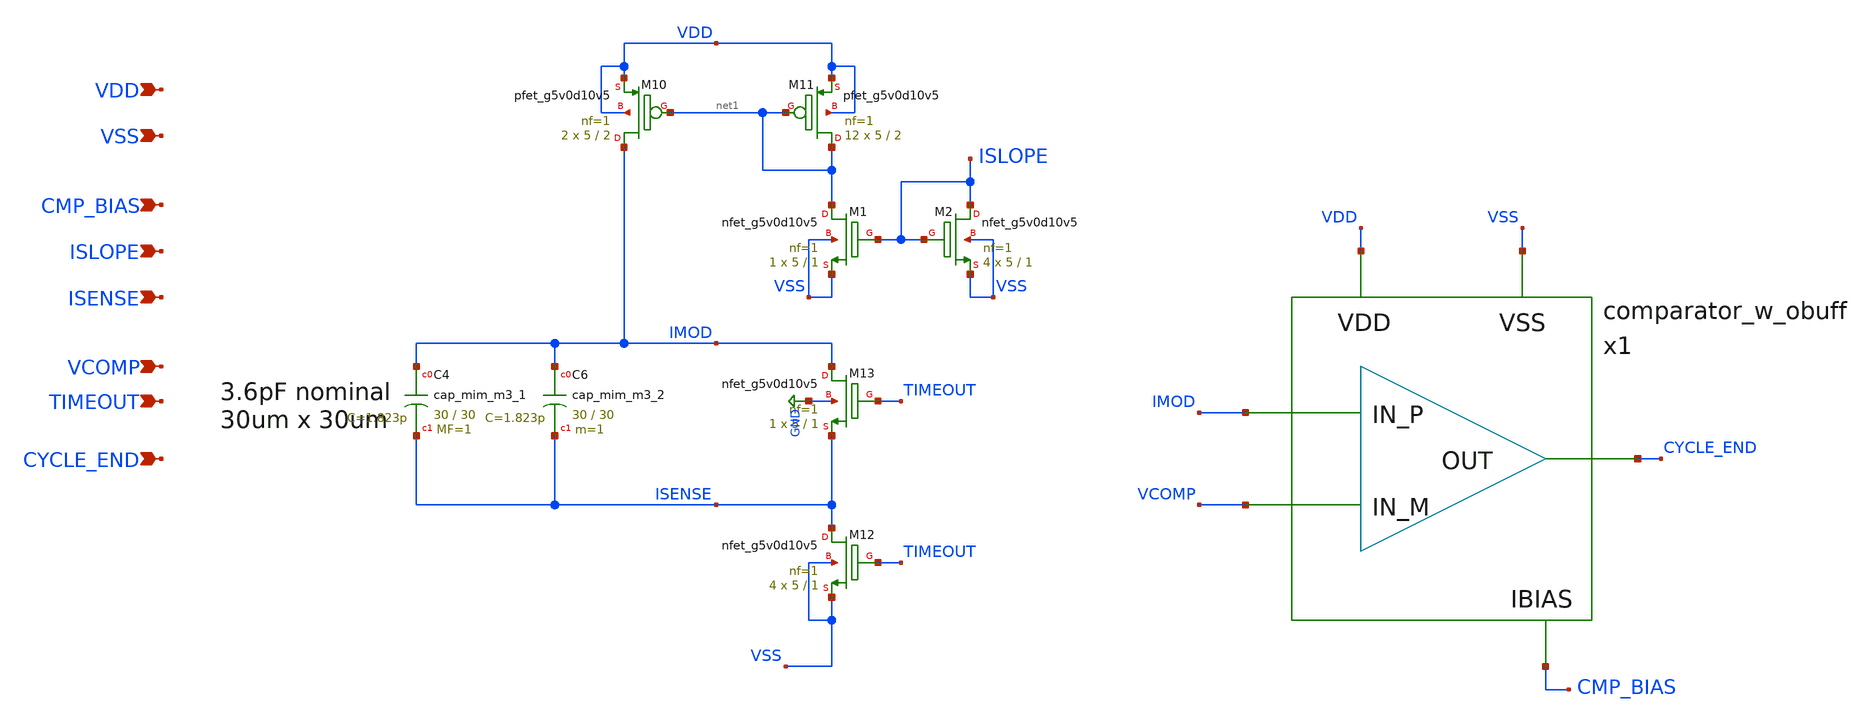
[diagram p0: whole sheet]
** sch_path: design/modulator/modulator.sch
**.subckt modulator ISENSE VCOMP TIMEOUT VDD VSS CMP_BIAS ISLOPE CYCLE_END
*.ipin ISENSE
*.ipin VCOMP
*.ipin TIMEOUT
*.ipin VDD
*.ipin VSS
*.ipin CMP_BIAS
*.ipin ISLOPE
*.ipin CYCLE_END
x1 IMOD VCOMP CYCLE_END VDD VSS CMP_BIAS comparator_w_obuff
XM10 IMOD net1 VDD VDD sky130_fd_pr__pfet_g5v0d10v5 L=2 W=5 nf=1 ad='int((nf+1)/2) * W/nf * 0.29' as='int((nf+2)/2) * W/nf * 0.29'
+ pd='2*int((nf+1)/2) * (W/nf + 0.29)' ps='2*int((nf+2)/2) * (W/nf + 0.29)' nrd='0.29 / W' nrs='0.29 / W'
+ sa=0 sb=0 sd=0 mult=2 m=2
XM11 net1 net1 VDD VDD sky130_fd_pr__pfet_g5v0d10v5 L=2 W=5 nf=1 ad='int((nf+1)/2) * W/nf * 0.29' as='int((nf+2)/2) * W/nf * 0.29'
+ pd='2*int((nf+1)/2) * (W/nf + 0.29)' ps='2*int((nf+2)/2) * (W/nf + 0.29)' nrd='0.29 / W' nrs='0.29 / W'
+ sa=0 sb=0 sd=0 mult=12 m=12
XM12 ISENSE TIMEOUT VSS VSS sky130_fd_pr__nfet_g5v0d10v5 L=1 W=5 nf=1 ad='int((nf+1)/2) * W/nf * 0.29'
+ as='int((nf+2)/2) * W/nf * 0.29' pd='2*int((nf+1)/2) * (W/nf + 0.29)' ps='2*int((nf+2)/2) * (W/nf + 0.29)'
+ nrd='0.29 / W' nrs='0.29 / W' sa=0 sb=0 sd=0 mult=4 m=4
XM13 IMOD TIMEOUT ISENSE GND sky130_fd_pr__nfet_g5v0d10v5 L=1 W=5 nf=1 ad='int((nf+1)/2) * W/nf * 0.29'
+ as='int((nf+2)/2) * W/nf * 0.29' pd='2*int((nf+1)/2) * (W/nf + 0.29)' ps='2*int((nf+2)/2) * (W/nf + 0.29)'
+ nrd='0.29 / W' nrs='0.29 / W' sa=0 sb=0 sd=0 mult=1 m=1
XC4 IMOD ISENSE sky130_fd_pr__cap_mim_m3_1 W=30 L=30 MF=1 m=1
XC6 IMOD ISENSE sky130_fd_pr__cap_mim_m3_2 W=30 L=30 MF=1 m=1
XM1 net1 ISLOPE VSS VSS sky130_fd_pr__nfet_g5v0d10v5 L=1 W=5 nf=1 ad='int((nf+1)/2) * W/nf * 0.29' as='int((nf+2)/2) * W/nf * 0.29'
+ pd='2*int((nf+1)/2) * (W/nf + 0.29)' ps='2*int((nf+2)/2) * (W/nf + 0.29)' nrd='0.29 / W' nrs='0.29 / W'
+ sa=0 sb=0 sd=0 mult=1 m=1
XM2 ISLOPE ISLOPE VSS VSS sky130_fd_pr__nfet_g5v0d10v5 L=1 W=5 nf=1 ad='int((nf+1)/2) * W/nf * 0.29'
+ as='int((nf+2)/2) * W/nf * 0.29' pd='2*int((nf+1)/2) * (W/nf + 0.29)' ps='2*int((nf+2)/2) * (W/nf + 0.29)'
+ nrd='0.29 / W' nrs='0.29 / W' sa=0 sb=0 sd=0 mult=4 m=4
**.ends

* expanding   symbol:  design/comparator/comparator_w_obuff.sym # of pins=6
** sym_path: design/comparator/comparator_w_obuff.sym
** sch_path: design/comparator/comparator_w_obuff.sch
.subckt comparator_w_obuff Vinp Vinm Vout VDD VSS IB
*.iopin VDD
*.iopin VSS
*.iopin Vout
*.iopin Vinp
*.iopin Vinm
*.iopin IB
XM11 net4 IB VDD VDD sky130_fd_pr__pfet_g5v0d10v5 L=1 W=5 nf=1 ad='int((nf+1)/2) * W/nf * 0.29' as='int((nf+2)/2) * W/nf * 0.29'
+ pd='2*int((nf+1)/2) * (W/nf + 0.29)' ps='2*int((nf+2)/2) * (W/nf + 0.29)' nrd='0.29 / W' nrs='0.29 / W'
+ sa=0 sb=0 sd=0 mult=4 m=4
XM8 VMID net1 VDD VDD sky130_fd_pr__pfet_g5v0d10v5 L=1 W=5 nf=1 ad='int((nf+1)/2) * W/nf * 0.29' as='int((nf+2)/2) * W/nf * 0.29'
+ pd='2*int((nf+1)/2) * (W/nf + 0.29)' ps='2*int((nf+2)/2) * (W/nf + 0.29)' nrd='0.29 / W' nrs='0.29 / W'
+ sa=0 sb=0 sd=0 mult=4 m=4
XM7 net1 net1 VDD VDD sky130_fd_pr__pfet_g5v0d10v5 L=1 W=5 nf=1 ad='int((nf+1)/2) * W/nf * 0.29' as='int((nf+2)/2) * W/nf * 0.29'
+ pd='2*int((nf+1)/2) * (W/nf + 0.29)' ps='2*int((nf+2)/2) * (W/nf + 0.29)' nrd='0.29 / W' nrs='0.29 / W'
+ sa=0 sb=0 sd=0 mult=4 m=4
XM2 net3 Vinm net4 VDD sky130_fd_pr__pfet_g5v0d10v5 L=1 W=5 nf=1 ad='int((nf+1)/2) * W/nf * 0.29' as='int((nf+2)/2) * W/nf * 0.29'
+ pd='2*int((nf+1)/2) * (W/nf + 0.29)' ps='2*int((nf+2)/2) * (W/nf + 0.29)' nrd='0.29 / W' nrs='0.29 / W'
+ sa=0 sb=0 sd=0 mult=4 m=4
XM1 net2 Vinp net4 VDD sky130_fd_pr__pfet_g5v0d10v5 L=1 W=5 nf=1 ad='int((nf+1)/2) * W/nf * 0.29' as='int((nf+2)/2) * W/nf * 0.29'
+ pd='2*int((nf+1)/2) * (W/nf + 0.29)' ps='2*int((nf+2)/2) * (W/nf + 0.29)' nrd='0.29 / W' nrs='0.29 / W'
+ sa=0 sb=0 sd=0 mult=4 m=4
XMmir IB IB VDD VDD sky130_fd_pr__pfet_g5v0d10v5 L=1 W=5 nf=1 ad='int((nf+1)/2) * W/nf * 0.29' as='int((nf+2)/2) * W/nf * 0.29'
+ pd='2*int((nf+1)/2) * (W/nf + 0.29)' ps='2*int((nf+2)/2) * (W/nf + 0.29)' nrd='0.29 / W' nrs='0.29 / W'
+ sa=0 sb=0 sd=0 mult=2 m=2
XM12 VMID net3 VSS VSS sky130_fd_pr__nfet_g5v0d10v5 L=1 W=5 nf=1 ad='int((nf+1)/2) * W/nf * 0.29' as='int((nf+2)/2) * W/nf * 0.29'
+ pd='2*int((nf+1)/2) * (W/nf + 0.29)' ps='2*int((nf+2)/2) * (W/nf + 0.29)' nrd='0.29 / W' nrs='0.29 / W'
+ sa=0 sb=0 sd=0 mult=4 m=4
XM4 net3 net3 VSS VSS sky130_fd_pr__nfet_g5v0d10v5 L=1 W=5 nf=1 ad='int((nf+1)/2) * W/nf * 0.29' as='int((nf+2)/2) * W/nf * 0.29'
+ pd='2*int((nf+1)/2) * (W/nf + 0.29)' ps='2*int((nf+2)/2) * (W/nf + 0.29)' nrd='0.29 / W' nrs='0.29 / W'
+ sa=0 sb=0 sd=0 mult=3 m=3
XM6 net2 net3 VSS VSS sky130_fd_pr__nfet_g5v0d10v5 L=1 W=5 nf=1 ad='int((nf+1)/2) * W/nf * 0.29' as='int((nf+2)/2) * W/nf * 0.29'
+ pd='2*int((nf+1)/2) * (W/nf + 0.29)' ps='2*int((nf+2)/2) * (W/nf + 0.29)' nrd='0.29 / W' nrs='0.29 / W'
+ sa=0 sb=0 sd=0 mult=4 m=4
XM5 net3 net2 VSS VSS sky130_fd_pr__nfet_g5v0d10v5 L=1 W=5 nf=1 ad='int((nf+1)/2) * W/nf * 0.29' as='int((nf+2)/2) * W/nf * 0.29'
+ pd='2*int((nf+1)/2) * (W/nf + 0.29)' ps='2*int((nf+2)/2) * (W/nf + 0.29)' nrd='0.29 / W' nrs='0.29 / W'
+ sa=0 sb=0 sd=0 mult=4 m=4
XM3 net2 net2 VSS VSS sky130_fd_pr__nfet_g5v0d10v5 L=1 W=5 nf=1 ad='int((nf+1)/2) * W/nf * 0.29' as='int((nf+2)/2) * W/nf * 0.29'
+ pd='2*int((nf+1)/2) * (W/nf + 0.29)' ps='2*int((nf+2)/2) * (W/nf + 0.29)' nrd='0.29 / W' nrs='0.29 / W'
+ sa=0 sb=0 sd=0 mult=3 m=3
XM9 net1 net2 VSS VSS sky130_fd_pr__nfet_g5v0d10v5 L=1 W=5 nf=1 ad='int((nf+1)/2) * W/nf * 0.29' as='int((nf+2)/2) * W/nf * 0.29'
+ pd='2*int((nf+1)/2) * (W/nf + 0.29)' ps='2*int((nf+2)/2) * (W/nf + 0.29)' nrd='0.29 / W' nrs='0.29 / W'
+ sa=0 sb=0 sd=0 mult=4 m=4
XM10 Vout VMID VDD VDD sky130_fd_pr__pfet_g5v0d10v5 L=0.5 W=5 nf=1 ad='int((nf+1)/2) * W/nf * 0.29' as='int((nf+2)/2) * W/nf * 0.29'
+ pd='2*int((nf+1)/2) * (W/nf + 0.29)' ps='2*int((nf+2)/2) * (W/nf + 0.29)' nrd='0.29 / W' nrs='0.29 / W'
+ sa=0 sb=0 sd=0 mult=1 m=1
XM13 Vout VMID VSS VSS sky130_fd_pr__nfet_g5v0d10v5 L=0.5 W=5 nf=1 ad='int((nf+1)/2) * W/nf * 0.29' as='int((nf+2)/2) * W/nf * 0.29'
+ pd='2*int((nf+1)/2) * (W/nf + 0.29)' ps='2*int((nf+2)/2) * (W/nf + 0.29)' nrd='0.29 / W' nrs='0.29 / W'
+ sa=0 sb=0 sd=0 mult=1 m=1
.ends

.GLOBAL GND
.end
